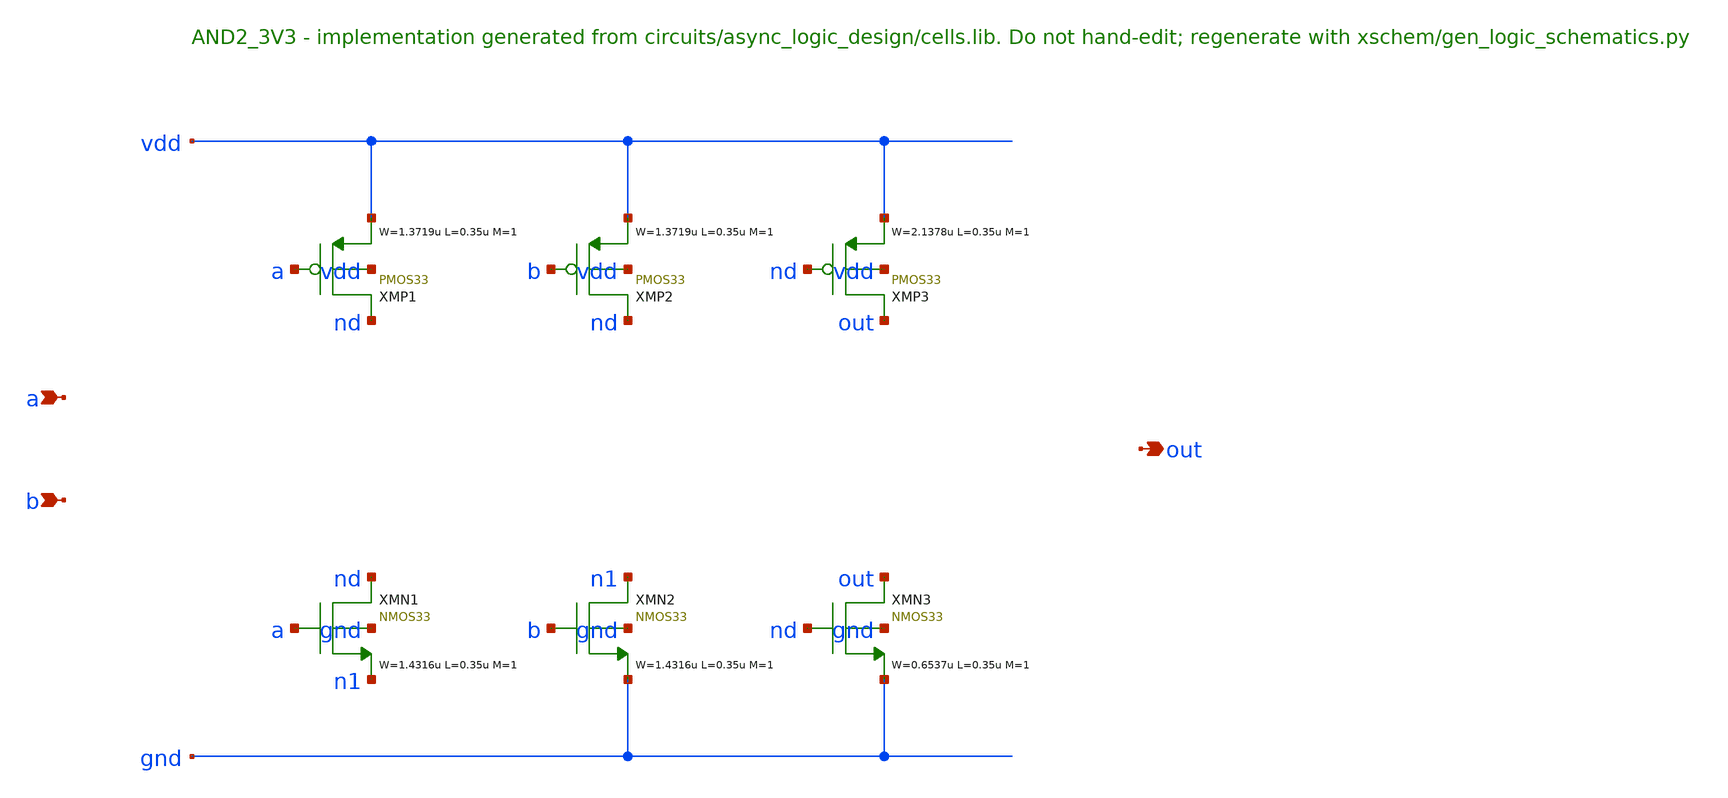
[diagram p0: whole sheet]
** sch_path: xschem/logic/AND2_3V3.sch
**.subckt AND2_3V3 a b out
*.ipin a
*.ipin b
*.opin out
XMP1 nd a vdd vdd PMOS33 W=1.3719u L=0.35u M=1 MM_SIGMA=0
XMP2 nd b vdd vdd PMOS33 W=1.3719u L=0.35u M=1 MM_SIGMA=0
XMP3 out nd vdd vdd PMOS33 W=2.1378u L=0.35u M=1 MM_SIGMA=0
XMN1 nd a n1 gnd NMOS33 W=1.4316u L=0.35u M=1 MM_SIGMA=0
XMN2 n1 b gnd gnd NMOS33 W=1.4316u L=0.35u M=1 MM_SIGMA=0
XMN3 out nd gnd gnd NMOS33 W=0.6537u L=0.35u M=1 MM_SIGMA=0
**.ends
.end
